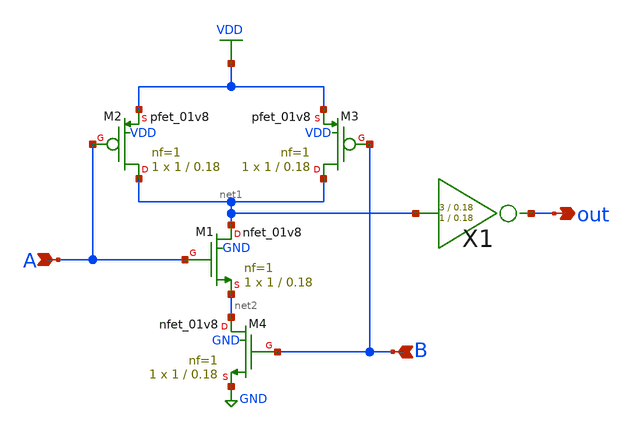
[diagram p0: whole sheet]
** sch_path: xschem/and_gate/and_gate.sch
**.subckt and_gate A B out
*.ipin A
*.ipin B
*.opin out
XM1 net1 A net2 GND sky130_fd_pr__nfet_01v8 L=0.18 W=1 nf=1 ad='int((nf+1)/2) * W/nf * 0.29' as='int((nf+2)/2) * W/nf * 0.29'
+ pd='2*int((nf+1)/2) * (W/nf + 0.29)' ps='2*int((nf+2)/2) * (W/nf + 0.29)' nrd='0.29 / W' nrs='0.29 / W'
+ sa=0 sb=0 sd=0 mult=1 m=1
XM2 net1 A VDD VDD sky130_fd_pr__pfet_01v8 L=0.18 W=1 nf=1 ad='int((nf+1)/2) * W/nf * 0.29' as='int((nf+2)/2) * W/nf * 0.29'
+ pd='2*int((nf+1)/2) * (W/nf + 0.29)' ps='2*int((nf+2)/2) * (W/nf + 0.29)' nrd='0.29 / W' nrs='0.29 / W'
+ sa=0 sb=0 sd=0 mult=1 m=1
XM3 net1 B VDD VDD sky130_fd_pr__pfet_01v8 L=0.18 W=1 nf=1 ad='int((nf+1)/2) * W/nf * 0.29' as='int((nf+2)/2) * W/nf * 0.29'
+ pd='2*int((nf+1)/2) * (W/nf + 0.29)' ps='2*int((nf+2)/2) * (W/nf + 0.29)' nrd='0.29 / W' nrs='0.29 / W'
+ sa=0 sb=0 sd=0 mult=1 m=1
XM4 net2 B GND GND sky130_fd_pr__nfet_01v8 L=0.18 W=1 nf=1 ad='int((nf+1)/2) * W/nf * 0.29' as='int((nf+2)/2) * W/nf * 0.29'
+ pd='2*int((nf+1)/2) * (W/nf + 0.29)' ps='2*int((nf+2)/2) * (W/nf + 0.29)' nrd='0.29 / W' nrs='0.29 / W'
+ sa=0 sb=0 sd=0 mult=1 m=1
X1 net1 out inv Wpmos=3 Lpmos=0.18 Wnmos=1 Lnmos=0.18
**.ends

* expanding   symbol:  inv/inv.sym # of pins=2
** sym_path: xschem/inv/inv.sym
** sch_path: xschem/inv/inv.sch
.subckt inv in out  Wpmos=3 Lpmos=0.18 Wnmos=1 Lnmos=0.18
*.ipin in
*.iopin out
XM1 out in GND GND sky130_fd_pr__nfet_01v8 L=Lnmos W=Wnmos nf=1 ad='int((nf+1)/2) * W/nf * 0.29' as='int((nf+2)/2) * W/nf * 0.29'
+ pd='2*int((nf+1)/2) * (W/nf + 0.29)' ps='2*int((nf+2)/2) * (W/nf + 0.29)' nrd='0.29 / W' nrs='0.29 / W'
+ sa=0 sb=0 sd=0 mult=1 m=1
XM2 out in VDD VDD sky130_fd_pr__pfet_01v8 L=Lpmos W=Wpmos nf=1 ad='int((nf+1)/2) * W/nf * 0.29' as='int((nf+2)/2) * W/nf * 0.29'
+ pd='2*int((nf+1)/2) * (W/nf + 0.29)' ps='2*int((nf+2)/2) * (W/nf + 0.29)' nrd='0.29 / W' nrs='0.29 / W'
+ sa=0 sb=0 sd=0 mult=1 m=1
.ends

.GLOBAL VDD
.GLOBAL GND
.end
